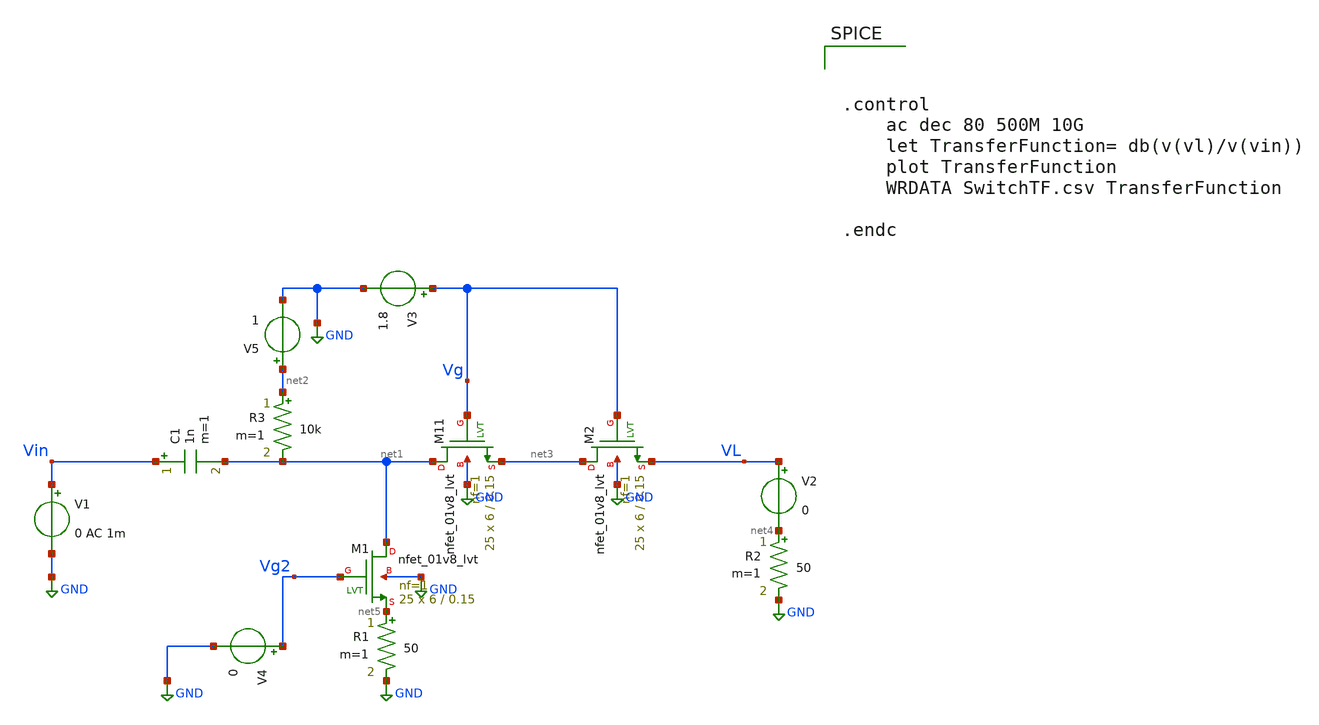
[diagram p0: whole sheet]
** sch_path: xschem/Switch_Characterization2.sch
**.subckt Switch_Characterization2
XM11 net1 Vg net3 GND sky130_fd_pr__nfet_01v8_lvt L=0.15 W=6 nf=1 ad='int((nf+1)/2) * W/nf * 0.29' as='int((nf+2)/2) * W/nf * 0.29'
+ pd='2*int((nf+1)/2) * (W/nf + 0.29)' ps='2*int((nf+2)/2) * (W/nf + 0.29)' nrd='0.29 / W' nrs='0.29 / W'
+ sa=0 sb=0 sd=0 mult=25 m=25
V1 Vin GND 0 AC 1m
R2 net4 GND 50 m=1
V2 VL net4 0
V3 Vg GND 1.8
XM1 net1 Vg2 net5 GND sky130_fd_pr__nfet_01v8_lvt L=0.15 W=6 nf=1 ad='int((nf+1)/2) * W/nf * 0.29' as='int((nf+2)/2) * W/nf * 0.29'
+ pd='2*int((nf+1)/2) * (W/nf + 0.29)' ps='2*int((nf+2)/2) * (W/nf + 0.29)' nrd='0.29 / W' nrs='0.29 / W'
+ sa=0 sb=0 sd=0 mult=25 m=25
R1 net5 GND 50 m=1
V4 Vg2 GND 0
C1 Vin net1 1n m=1
R3 net2 net1 10k m=1
V5 net2 GND 1
XM2 net3 Vg VL GND sky130_fd_pr__nfet_01v8_lvt L=0.15 W=6 nf=1 ad='int((nf+1)/2) * W/nf * 0.29' as='int((nf+2)/2) * W/nf * 0.29'
+ pd='2*int((nf+1)/2) * (W/nf + 0.29)' ps='2*int((nf+2)/2) * (W/nf + 0.29)' nrd='0.29 / W' nrs='0.29 / W'
+ sa=0 sb=0 sd=0 mult=25 m=25
**** begin user architecture code

.lib $::SKYWATER_MODELS/sky130.lib.spice tt




.control
	ac dec 80 500M 10G
	let TransferFunction= db(v(vl)/v(vin))
	plot TransferFunction
	WRDATA SwitchTF.csv TransferFunction

.endc


**** end user architecture code
**.ends
.GLOBAL GND
.end
